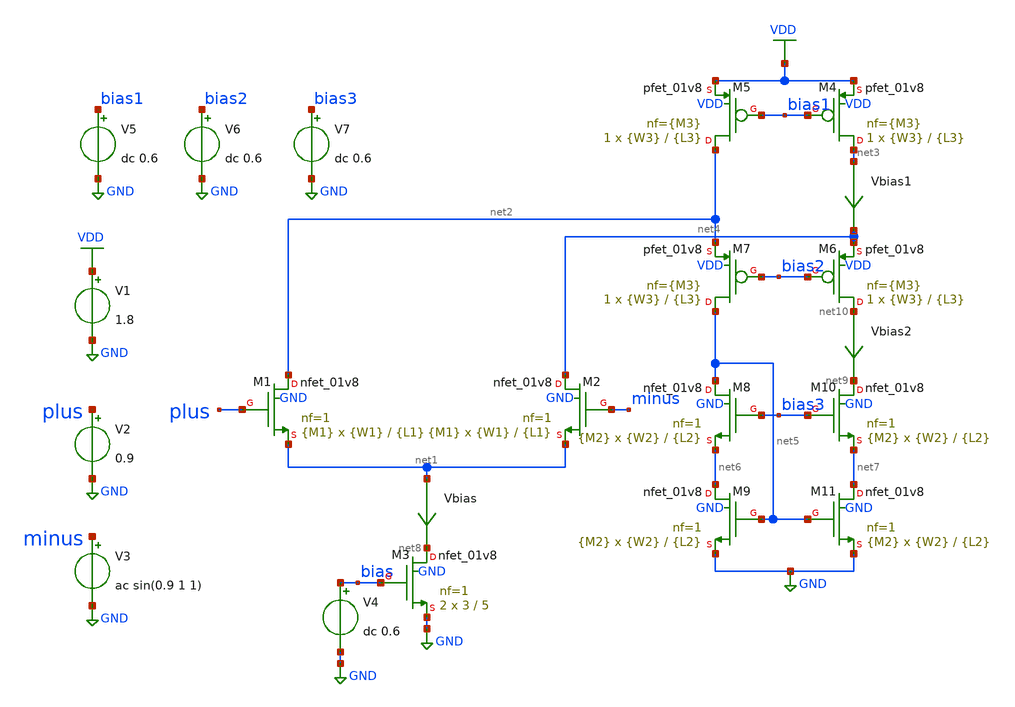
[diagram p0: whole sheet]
** sch_path: xschem/op3.sch
**.subckt op3
V4 bias GND dc 0.6
XM1 net2 plus net1 GND sky130_fd_pr__nfet_01v8 L={L1} W={W1} nf=1 ad='int((nf+1)/2) * W/nf * 0.29' as='int((nf+2)/2) * W/nf * 0.29'
+ pd='2*int((nf+1)/2) * (W/nf + 0.29)' ps='2*int((nf+2)/2) * (W/nf + 0.29)' nrd='0.29 / W' nrs='0.29 / W'
+ sa=0 sb=0 sd=0 mult={M1} m={M1}
XM3 net8 bias GND GND sky130_fd_pr__nfet_01v8 L=5 W=3 nf=1 ad='int((nf+1)/2) * W/nf * 0.29' as='int((nf+2)/2) * W/nf * 0.29'
+ pd='2*int((nf+1)/2) * (W/nf + 0.29)' ps='2*int((nf+2)/2) * (W/nf + 0.29)' nrd='0.29 / W' nrs='0.29 / W'
+ sa=0 sb=0 sd=0 mult=2 m=2
V1 VDD GND 1.8
V2 plus GND 0.9
V3 minus GND ac sin(0.9 1 1)
Vbias net1 net8 0
.save i(vbias)
XM2 net4 minus net1 GND sky130_fd_pr__nfet_01v8 L={L1} W={W1} nf=1 ad='int((nf+1)/2) * W/nf * 0.29' as='int((nf+2)/2) * W/nf * 0.29'
+ pd='2*int((nf+1)/2) * (W/nf + 0.29)' ps='2*int((nf+2)/2) * (W/nf + 0.29)' nrd='0.29 / W' nrs='0.29 / W'
+ sa=0 sb=0 sd=0 mult={M1} m={M1}
XM7 net5 bias2 net2 VDD sky130_fd_pr__pfet_01v8 L={L3} W={W3} nf={M3} ad='int((nf+1)/2) * W/nf * 0.29'
+ as='int((nf+2)/2) * W/nf * 0.29' pd='2*int((nf+1)/2) * (W/nf + 0.29)' ps='2*int((nf+2)/2) * (W/nf + 0.29)'
+ nrd='0.29 / W' nrs='0.29 / W' sa=0 sb=0 sd=0 mult=1 m=1
XM8 net5 bias3 net6 GND sky130_fd_pr__nfet_01v8 L={L2} W={W2} nf=1 ad='int((nf+1)/2) * W/nf * 0.29' as='int((nf+2)/2) * W/nf * 0.29'
+ pd='2*int((nf+1)/2) * (W/nf + 0.29)' ps='2*int((nf+2)/2) * (W/nf + 0.29)' nrd='0.29 / W' nrs='0.29 / W'
+ sa=0 sb=0 sd=0 mult={M2} m={M2}
XM9 net6 net5 GND GND sky130_fd_pr__nfet_01v8 L={L2} W={W2} nf=1 ad='int((nf+1)/2) * W/nf * 0.29' as='int((nf+2)/2) * W/nf * 0.29'
+ pd='2*int((nf+1)/2) * (W/nf + 0.29)' ps='2*int((nf+2)/2) * (W/nf + 0.29)' nrd='0.29 / W' nrs='0.29 / W'
+ sa=0 sb=0 sd=0 mult={M2} m={M2}
XM10 net9 bias3 net7 GND sky130_fd_pr__nfet_01v8 L={L2} W={W2} nf=1 ad='int((nf+1)/2) * W/nf * 0.29'
+ as='int((nf+2)/2) * W/nf * 0.29' pd='2*int((nf+1)/2) * (W/nf + 0.29)' ps='2*int((nf+2)/2) * (W/nf + 0.29)'
+ nrd='0.29 / W' nrs='0.29 / W' sa=0 sb=0 sd=0 mult={M2} m={M2}
XM11 net7 net5 GND GND sky130_fd_pr__nfet_01v8 L={L2} W={W2} nf=1 ad='int((nf+1)/2) * W/nf * 0.29' as='int((nf+2)/2) * W/nf * 0.29'
+ pd='2*int((nf+1)/2) * (W/nf + 0.29)' ps='2*int((nf+2)/2) * (W/nf + 0.29)' nrd='0.29 / W' nrs='0.29 / W'
+ sa=0 sb=0 sd=0 mult={M2} m={M2}
XM6 net10 bias2 net4 VDD sky130_fd_pr__pfet_01v8 L={L3} W={W3} nf={M3} ad='int((nf+1)/2) * W/nf * 0.29'
+ as='int((nf+2)/2) * W/nf * 0.29' pd='2*int((nf+1)/2) * (W/nf + 0.29)' ps='2*int((nf+2)/2) * (W/nf + 0.29)'
+ nrd='0.29 / W' nrs='0.29 / W' sa=0 sb=0 sd=0 mult=1 m=1
XM4 net3 bias1 VDD VDD sky130_fd_pr__pfet_01v8 L={L3} W={W3} nf={M3} ad='int((nf+1)/2) * W/nf * 0.29'
+ as='int((nf+2)/2) * W/nf * 0.29' pd='2*int((nf+1)/2) * (W/nf + 0.29)' ps='2*int((nf+2)/2) * (W/nf + 0.29)'
+ nrd='0.29 / W' nrs='0.29 / W' sa=0 sb=0 sd=0 mult=1 m=1
XM5 net2 bias1 VDD VDD sky130_fd_pr__pfet_01v8 L={L3} W={W3} nf={M3} ad='int((nf+1)/2) * W/nf * 0.29'
+ as='int((nf+2)/2) * W/nf * 0.29' pd='2*int((nf+1)/2) * (W/nf + 0.29)' ps='2*int((nf+2)/2) * (W/nf + 0.29)'
+ nrd='0.29 / W' nrs='0.29 / W' sa=0 sb=0 sd=0 mult=1 m=1
V5 bias1 GND dc 0.6
V6 bias2 GND dc 0.6
V7 bias3 GND dc 0.6
Vbias1 net3 net4 0
.save i(vbias1)
Vbias2 net10 net9 0
.save i(vbias2)
**** begin user architecture code


.param L1=1
.param W1=1
.param M1=2
.param L2=1
.param W2=2
.param M2=2
.param L3=1
.param W3=5
.param M3=2




.option savecurrents
.control
save all
op
remzerovec
write op3.raw
set appendwrite
dc v4 0 1.8 0.1
plot i(vbias) i(vbias1) i(vbias2)

.endc



** opencircuitdesign pdks install
.lib $::SKYWATER_MODELS/sky130.lib.spice tt


**** end user architecture code
**.ends
.GLOBAL GND
.GLOBAL VDD
.end
